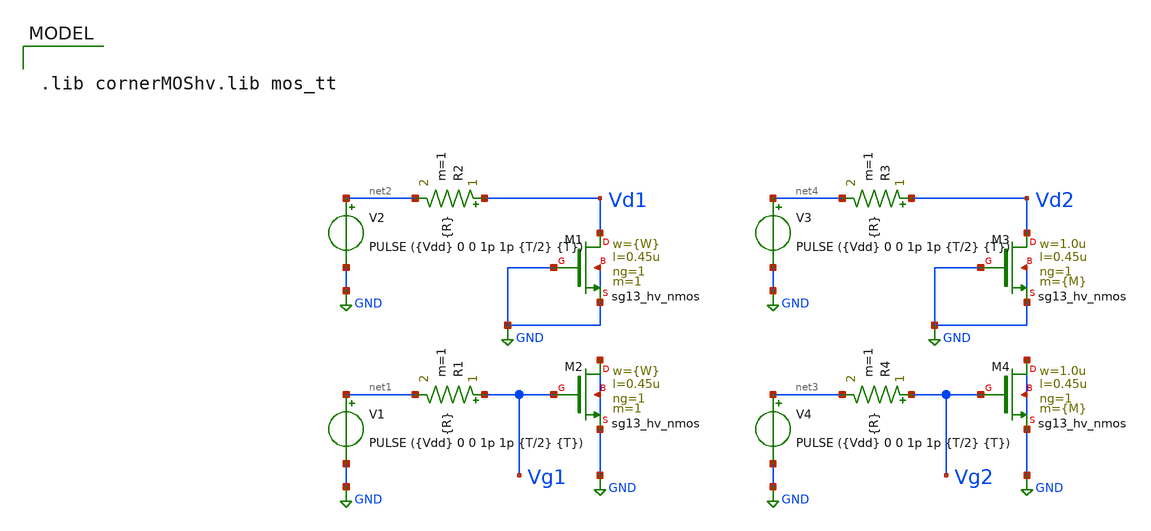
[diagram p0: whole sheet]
** sch_path: xschem/CMOS_Char/Cap_HvMOS.sch
**.subckt Cap_HvMOS
R2 Vd1 net2 {R} m=1
V2 net2 GND PULSE ({Vdd} 0 0 1p 1p {T/2} {T})
XM1 Vd1 GND GND GND sg13_hv_nmos w={W} l=0.45u ng=1 m=1 mm_ok=1
R1 Vg1 net1 {R} m=1
V1 net1 GND PULSE ({Vdd} 0 0 1p 1p {T/2} {T})
XM2 GND Vg1 GND GND sg13_hv_nmos w={W} l=0.45u ng=1 m=1 mm_ok=1
R3 Vd2 net4 {R} m=1
V3 net4 GND PULSE ({Vdd} 0 0 1p 1p {T/2} {T})
XM3 Vd2 GND GND GND sg13_hv_nmos w=1.0u l=0.45u ng=1 m={M} mm_ok=1
R4 Vg2 net3 {R} m=1
V4 net3 GND PULSE ({Vdd} 0 0 1p 1p {T/2} {T})
XM4 GND Vg2 GND GND sg13_hv_nmos w=1.0u l=0.45u ng=1 m={M} mm_ok=1
**** begin user architecture code



.control
tran 10p 10n
meas tran tau_d1 when v(Vd1) = 2.079 CROSS=1
meas tran tau_g1 when v(Vg1) = 2.079 CROSS=1
meas tran tau_d2 when v(Vd2) = 2.079 CROSS=1
meas tran tau_g2 when v(Vg2) = 2.079 CROSS=1

let cd1 = tau_d1/(100k)
let cg1 = tau_g1/(100k)
let cd2 = tau_d2/(100k)
let cg2 = tau_g2/(100k)

print cd1 cd2
print cg1 cg2

.endc



.lib cornerMOShv.lib mos_tt



.param R = 100k
.param Vdd = 3.3
.param T = 8n
.param M = 10
.param W = {M*1u}


**** end user architecture code
**.ends
.GLOBAL GND
.end
